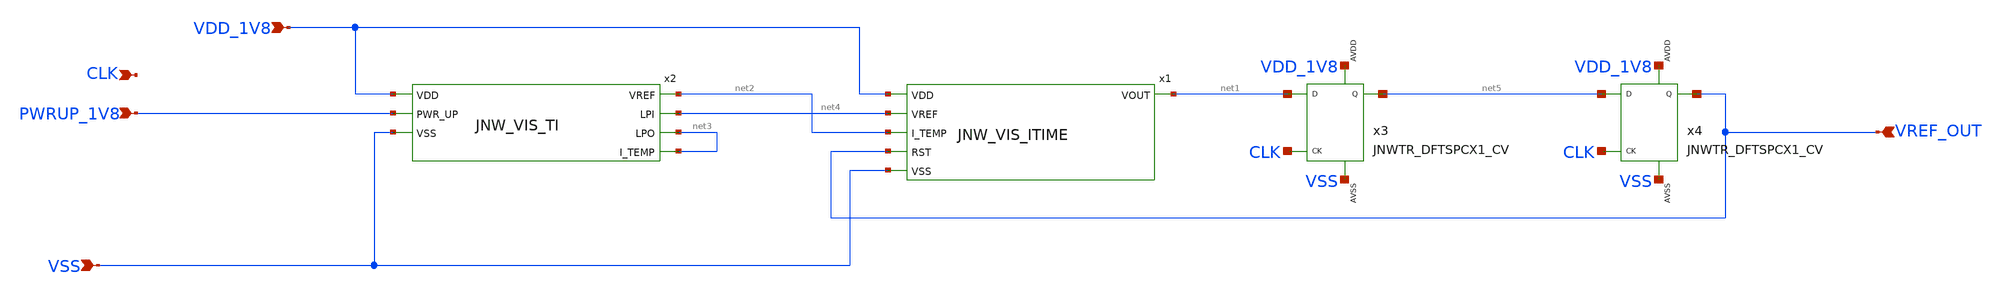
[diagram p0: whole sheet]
** sch_path: design/JNW_GR02_SKY130A/JNW_GR02_temperature.sch
**.subckt JNW_GR02_temperature VDD_1V8 VSS PWRUP_1V8 CLK VREF_OUT
*.ipin VDD_1V8
*.ipin VSS
*.ipin PWRUP_1V8
*.ipin CLK
*.ipin VREF_OUT
x1 VDD_1V8 net4 net1 net2 VREF_OUT VSS JNW_VIS_ITIME
x2 VDD_1V8 net2 net4 net3 net3 PWRUP_1V8 VSS JNW_VIS_TI
x3 net1 CLK net5 VDD_1V8 VSS JNWTR_DFTSPCX1_CV xoffset=0 yoffset=0 angle=0
x4 net5 CLK VREF_OUT VDD_1V8 VSS JNWTR_DFTSPCX1_CV xoffset=0 yoffset=0 angle=0
**.ends
.end
